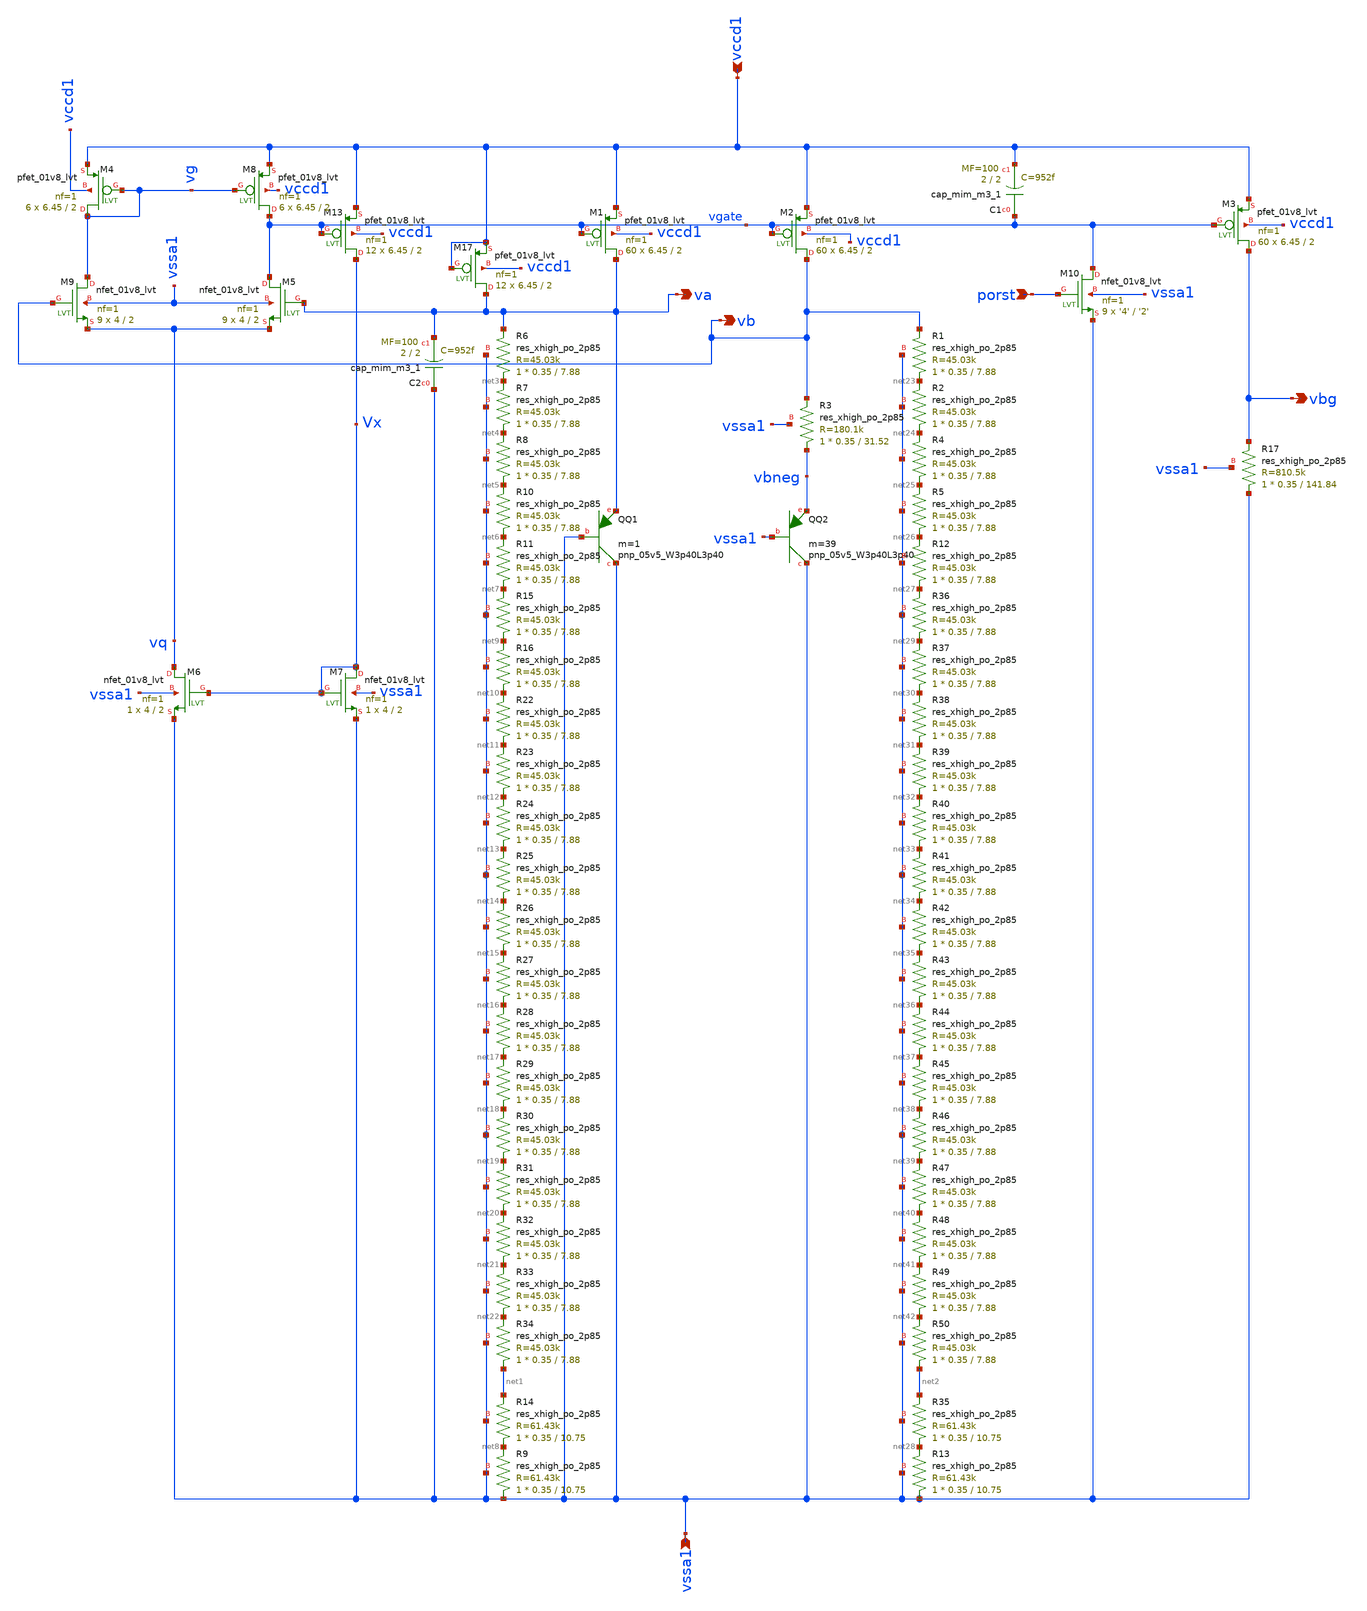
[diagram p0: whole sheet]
** sch_path: xschem/xschem/tsmc_bandgap_real_lvs.sch
**.subckt tsmc_bandgap_real_lvs porst vbg va vb vccd1 vssa1
*.ipin porst
*.opin vbg
*.opin va
*.opin vb
*.ipin vccd1
*.ipin vssa1
XM5 vgate va vq vssa1 sky130_fd_pr__nfet_01v8_lvt L=2 W=4 nf=1 ad='int((nf+1)/2) * W/nf * 0.29' as='int((nf+2)/2) * W/nf * 0.29'
+ pd='2*int((nf+1)/2) * (W/nf + 0.29)' ps='2*int((nf+2)/2) * (W/nf + 0.29)' nrd='0.29 / W' nrs='0.29 / W'
+ sa=0 sb=0 sd=0 mult=9 m=9
XM6 vq Vx vssa1 vssa1 sky130_fd_pr__nfet_01v8_lvt L=2 W=4 nf=1 ad='int((nf+1)/2) * W/nf * 0.29' as='int((nf+2)/2) * W/nf * 0.29'
+ pd='2*int((nf+1)/2) * (W/nf + 0.29)' ps='2*int((nf+2)/2) * (W/nf + 0.29)' nrd='0.29 / W' nrs='0.29 / W'
+ sa=0 sb=0 sd=0 mult=1 m=1
XM9 vg vb vq vssa1 sky130_fd_pr__nfet_01v8_lvt L=2 W=4 nf=1 ad='int((nf+1)/2) * W/nf * 0.29' as='int((nf+2)/2) * W/nf * 0.29'
+ pd='2*int((nf+1)/2) * (W/nf + 0.29)' ps='2*int((nf+2)/2) * (W/nf + 0.29)' nrd='0.29 / W' nrs='0.29 / W'
+ sa=0 sb=0 sd=0 mult=9 m=9
XM7 Vx Vx vssa1 vssa1 sky130_fd_pr__nfet_01v8_lvt L=2 W=4 nf=1 ad='int((nf+1)/2) * W/nf * 0.29' as='int((nf+2)/2) * W/nf * 0.29'
+ pd='2*int((nf+1)/2) * (W/nf + 0.29)' ps='2*int((nf+2)/2) * (W/nf + 0.29)' nrd='0.29 / W' nrs='0.29 / W'
+ sa=0 sb=0 sd=0 mult=1 m=1
XM13 Vx vgate vccd1 vccd1 sky130_fd_pr__pfet_01v8_lvt L=2 W=6.45 nf=1 ad='int((nf+1)/2) * W/nf * 0.29'
+ as='int((nf+2)/2) * W/nf * 0.29' pd='2*int((nf+1)/2) * (W/nf + 0.29)' ps='2*int((nf+2)/2) * (W/nf + 0.29)'
+ nrd='0.29 / W' nrs='0.29 / W' sa=0 sb=0 sd=0 mult=12 m=12
XM1 va vgate vccd1 vccd1 sky130_fd_pr__pfet_01v8_lvt L=2 W=6.45 nf=1 ad='int((nf+1)/2) * W/nf * 0.29'
+ as='int((nf+2)/2) * W/nf * 0.29' pd='2*int((nf+1)/2) * (W/nf + 0.29)' ps='2*int((nf+2)/2) * (W/nf + 0.29)'
+ nrd='0.29 / W' nrs='0.29 / W' sa=0 sb=0 sd=0 mult=60 m=60
XM2 vb vgate vccd1 vccd1 sky130_fd_pr__pfet_01v8_lvt L=2 W=6.45 nf=1 ad='int((nf+1)/2) * W/nf * 0.29'
+ as='int((nf+2)/2) * W/nf * 0.29' pd='2*int((nf+1)/2) * (W/nf + 0.29)' ps='2*int((nf+2)/2) * (W/nf + 0.29)'
+ nrd='0.29 / W' nrs='0.29 / W' sa=0 sb=0 sd=0 mult=60 m=60
XM3 vbg vgate vccd1 vccd1 sky130_fd_pr__pfet_01v8_lvt L=2 W=6.45 nf=1 ad='int((nf+1)/2) * W/nf * 0.29'
+ as='int((nf+2)/2) * W/nf * 0.29' pd='2*int((nf+1)/2) * (W/nf + 0.29)' ps='2*int((nf+2)/2) * (W/nf + 0.29)'
+ nrd='0.29 / W' nrs='0.29 / W' sa=0 sb=0 sd=0 mult=60 m=60
XM4 vg vg vccd1 vccd1 sky130_fd_pr__pfet_01v8_lvt L=2 W=6.45 nf=1 ad='int((nf+1)/2) * W/nf * 0.29' as='int((nf+2)/2) * W/nf * 0.29'
+ pd='2*int((nf+1)/2) * (W/nf + 0.29)' ps='2*int((nf+2)/2) * (W/nf + 0.29)' nrd='0.29 / W' nrs='0.29 / W'
+ sa=0 sb=0 sd=0 mult=6 m=6
XM8 vgate vg vccd1 vccd1 sky130_fd_pr__pfet_01v8_lvt L=2 W=6.45 nf=1 ad='int((nf+1)/2) * W/nf * 0.29'
+ as='int((nf+2)/2) * W/nf * 0.29' pd='2*int((nf+1)/2) * (W/nf + 0.29)' ps='2*int((nf+2)/2) * (W/nf + 0.29)'
+ nrd='0.29 / W' nrs='0.29 / W' sa=0 sb=0 sd=0 mult=6 m=6
XM10 vgate porst vssa1 vssa1 sky130_fd_pr__nfet_01v8_lvt L='2' W='4' nf=1 ad='int((nf+1)/2) * W/nf * 0.29'
+ as='int((nf+2)/2) * W/nf * 0.29' pd='2*int((nf+1)/2) * (W/nf + 0.29)' ps='2*int((nf+2)/2) * (W/nf + 0.29)'
+ nrd='0.29 / W' nrs='0.29 / W' sa=0 sb=0 sd=0 mult=9 m=9
XR6 net3 va vssa1 sky130_fd_pr__res_xhigh_po_2p85 L=7.88 mult=1 m=1
XR7 net4 net3 vssa1 sky130_fd_pr__res_xhigh_po_2p85 L=7.88 mult=1 m=1
XR8 net5 net4 vssa1 sky130_fd_pr__res_xhigh_po_2p85 L=7.88 mult=1 m=1
XR10 net6 net5 vssa1 sky130_fd_pr__res_xhigh_po_2p85 L=7.88 mult=1 m=1
XR11 net7 net6 vssa1 sky130_fd_pr__res_xhigh_po_2p85 L=7.88 mult=1 m=1
XR9 vssa1 net8 vssa1 sky130_fd_pr__res_xhigh_po_2p85 L=10.75 mult=1 m=1
XR3 vbneg vb vssa1 sky130_fd_pr__res_xhigh_po_2p85 L=31.52 mult=1 m=1
XR17 vssa1 vbg vssa1 sky130_fd_pr__res_xhigh_po_2p85 L=141.84 mult=1 m=1
XM17 va vccd1 vccd1 vccd1 sky130_fd_pr__pfet_01v8_lvt L=2 W=6.45 nf=1 ad='int((nf+1)/2) * W/nf * 0.29'
+ as='int((nf+2)/2) * W/nf * 0.29' pd='2*int((nf+1)/2) * (W/nf + 0.29)' ps='2*int((nf+2)/2) * (W/nf + 0.29)'
+ nrd='0.29 / W' nrs='0.29 / W' sa=0 sb=0 sd=0 mult=12 m=12
XC1 vgate vccd1 sky130_fd_pr__cap_mim_m3_1 W=2 L=2 MF=100 m=100
XQQ1 vssa1 vssa1 va sky130_fd_pr__pnp_05v5_W3p40L3p40 m=1
XQQ2 vssa1 vssa1 vbneg sky130_fd_pr__pnp_05v5_W3p40L3p40 m=39
XC2 vssa1 va sky130_fd_pr__cap_mim_m3_1 W=2 L=2 MF=100 m=100
XR14 net8 net1 vssa1 sky130_fd_pr__res_xhigh_po_2p85 L=10.75 mult=1 m=1
XR15 net9 net7 vssa1 sky130_fd_pr__res_xhigh_po_2p85 L=7.88 mult=1 m=1
XR16 net10 net9 vssa1 sky130_fd_pr__res_xhigh_po_2p85 L=7.88 mult=1 m=1
XR22 net11 net10 vssa1 sky130_fd_pr__res_xhigh_po_2p85 L=7.88 mult=1 m=1
XR23 net12 net11 vssa1 sky130_fd_pr__res_xhigh_po_2p85 L=7.88 mult=1 m=1
XR24 net13 net12 vssa1 sky130_fd_pr__res_xhigh_po_2p85 L=7.88 mult=1 m=1
XR25 net14 net13 vssa1 sky130_fd_pr__res_xhigh_po_2p85 L=7.88 mult=1 m=1
XR26 net15 net14 vssa1 sky130_fd_pr__res_xhigh_po_2p85 L=7.88 mult=1 m=1
XR27 net16 net15 vssa1 sky130_fd_pr__res_xhigh_po_2p85 L=7.88 mult=1 m=1
XR28 net17 net16 vssa1 sky130_fd_pr__res_xhigh_po_2p85 L=7.88 mult=1 m=1
XR29 net18 net17 vssa1 sky130_fd_pr__res_xhigh_po_2p85 L=7.88 mult=1 m=1
XR30 net19 net18 vssa1 sky130_fd_pr__res_xhigh_po_2p85 L=7.88 mult=1 m=1
XR31 net20 net19 vssa1 sky130_fd_pr__res_xhigh_po_2p85 L=7.88 mult=1 m=1
XR32 net21 net20 vssa1 sky130_fd_pr__res_xhigh_po_2p85 L=7.88 mult=1 m=1
XR33 net22 net21 vssa1 sky130_fd_pr__res_xhigh_po_2p85 L=7.88 mult=1 m=1
XR34 net1 net22 vssa1 sky130_fd_pr__res_xhigh_po_2p85 L=7.88 mult=1 m=1
XR1 net23 vb vssa1 sky130_fd_pr__res_xhigh_po_2p85 L=7.88 mult=1 m=1
XR2 net24 net23 vssa1 sky130_fd_pr__res_xhigh_po_2p85 L=7.88 mult=1 m=1
XR4 net25 net24 vssa1 sky130_fd_pr__res_xhigh_po_2p85 L=7.88 mult=1 m=1
XR5 net26 net25 vssa1 sky130_fd_pr__res_xhigh_po_2p85 L=7.88 mult=1 m=1
XR12 net27 net26 vssa1 sky130_fd_pr__res_xhigh_po_2p85 L=7.88 mult=1 m=1
XR13 vssa1 net28 vssa1 sky130_fd_pr__res_xhigh_po_2p85 L=10.75 mult=1 m=1
XR35 net28 net2 vssa1 sky130_fd_pr__res_xhigh_po_2p85 L=10.75 mult=1 m=1
XR36 net29 net27 vssa1 sky130_fd_pr__res_xhigh_po_2p85 L=7.88 mult=1 m=1
XR37 net30 net29 vssa1 sky130_fd_pr__res_xhigh_po_2p85 L=7.88 mult=1 m=1
XR38 net31 net30 vssa1 sky130_fd_pr__res_xhigh_po_2p85 L=7.88 mult=1 m=1
XR39 net32 net31 vssa1 sky130_fd_pr__res_xhigh_po_2p85 L=7.88 mult=1 m=1
XR40 net33 net32 vssa1 sky130_fd_pr__res_xhigh_po_2p85 L=7.88 mult=1 m=1
XR41 net34 net33 vssa1 sky130_fd_pr__res_xhigh_po_2p85 L=7.88 mult=1 m=1
XR42 net35 net34 vssa1 sky130_fd_pr__res_xhigh_po_2p85 L=7.88 mult=1 m=1
XR43 net36 net35 vssa1 sky130_fd_pr__res_xhigh_po_2p85 L=7.88 mult=1 m=1
XR44 net37 net36 vssa1 sky130_fd_pr__res_xhigh_po_2p85 L=7.88 mult=1 m=1
XR45 net38 net37 vssa1 sky130_fd_pr__res_xhigh_po_2p85 L=7.88 mult=1 m=1
XR46 net39 net38 vssa1 sky130_fd_pr__res_xhigh_po_2p85 L=7.88 mult=1 m=1
XR47 net40 net39 vssa1 sky130_fd_pr__res_xhigh_po_2p85 L=7.88 mult=1 m=1
XR48 net41 net40 vssa1 sky130_fd_pr__res_xhigh_po_2p85 L=7.88 mult=1 m=1
XR49 net42 net41 vssa1 sky130_fd_pr__res_xhigh_po_2p85 L=7.88 mult=1 m=1
XR50 net2 net42 vssa1 sky130_fd_pr__res_xhigh_po_2p85 L=7.88 mult=1 m=1
**.ends
.end
